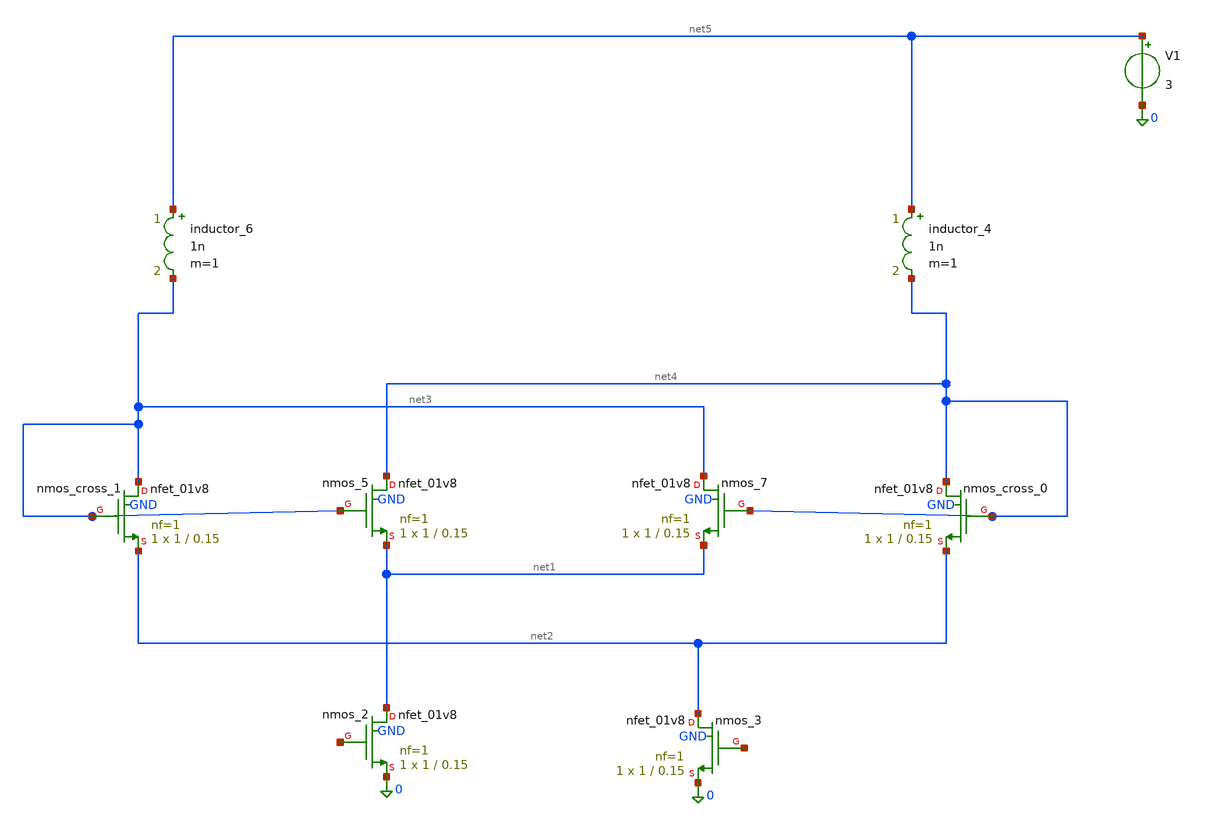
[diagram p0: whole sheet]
** sch_path: golden_netlists/10_1007_s10470-024-02258-z_02_001.sch
**.subckt 10_1007_s10470-024-02258-z_02_001
inductor_4 net5 net4 1n m=1
inductor_6 net5 net3 1n m=1
Xnmos_2 net1 net6 0 GND sky130_fd_pr__nfet_01v8 L=0.15 W=1 nf=1 ad='int((nf+1)/2) * W/nf * 0.29' as='int((nf+2)/2) * W/nf * 0.29'
+ pd='2*int((nf+1)/2) * (W/nf + 0.29)' ps='2*int((nf+2)/2) * (W/nf + 0.29)' nrd='0.29 / W' nrs='0.29 / W'
+ sa=0 sb=0 sd=0 mult=1 m=1
Xnmos_3 net2 net7 0 GND sky130_fd_pr__nfet_01v8 L=0.15 W=1 nf=1 ad='int((nf+1)/2) * W/nf * 0.29' as='int((nf+2)/2) * W/nf * 0.29'
+ pd='2*int((nf+1)/2) * (W/nf + 0.29)' ps='2*int((nf+2)/2) * (W/nf + 0.29)' nrd='0.29 / W' nrs='0.29 / W'
+ sa=0 sb=0 sd=0 mult=1 m=1
Xnmos_5 net4 net3 net1 GND sky130_fd_pr__nfet_01v8 L=0.15 W=1 nf=1 ad='int((nf+1)/2) * W/nf * 0.29' as='int((nf+2)/2) * W/nf * 0.29'
+ pd='2*int((nf+1)/2) * (W/nf + 0.29)' ps='2*int((nf+2)/2) * (W/nf + 0.29)' nrd='0.29 / W' nrs='0.29 / W'
+ sa=0 sb=0 sd=0 mult=1 m=1
Xnmos_7 net3 net4 net1 GND sky130_fd_pr__nfet_01v8 L=0.15 W=1 nf=1 ad='int((nf+1)/2) * W/nf * 0.29' as='int((nf+2)/2) * W/nf * 0.29'
+ pd='2*int((nf+1)/2) * (W/nf + 0.29)' ps='2*int((nf+2)/2) * (W/nf + 0.29)' nrd='0.29 / W' nrs='0.29 / W'
+ sa=0 sb=0 sd=0 mult=1 m=1
Xnmos_cross_0 net4 net4 net2 GND sky130_fd_pr__nfet_01v8 L=0.15 W=1 nf=1 ad='int((nf+1)/2) * W/nf * 0.29'
+ as='int((nf+2)/2) * W/nf * 0.29' pd='2*int((nf+1)/2) * (W/nf + 0.29)' ps='2*int((nf+2)/2) * (W/nf + 0.29)'
+ nrd='0.29 / W' nrs='0.29 / W' sa=0 sb=0 sd=0 mult=1 m=1
Xnmos_cross_1 net3 net3 net2 GND sky130_fd_pr__nfet_01v8 L=0.15 W=1 nf=1 ad='int((nf+1)/2) * W/nf * 0.29'
+ as='int((nf+2)/2) * W/nf * 0.29' pd='2*int((nf+1)/2) * (W/nf + 0.29)' ps='2*int((nf+2)/2) * (W/nf + 0.29)'
+ nrd='0.29 / W' nrs='0.29 / W' sa=0 sb=0 sd=0 mult=1 m=1
V1 net5 0 3
**.ends
.end
